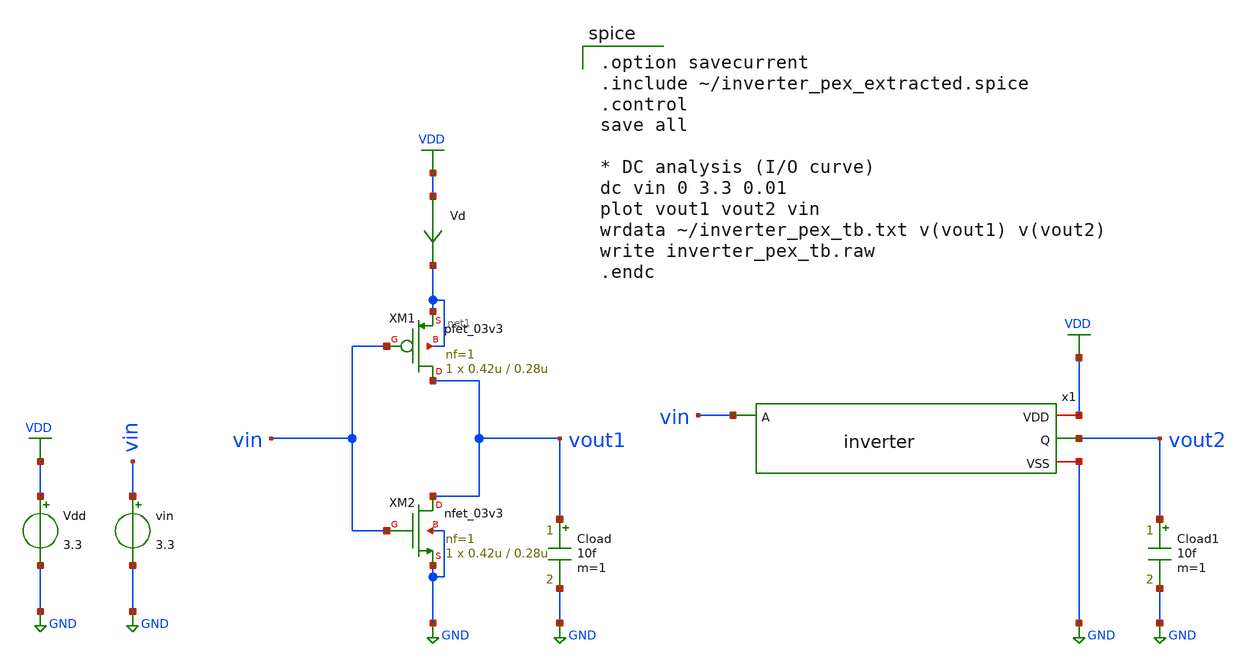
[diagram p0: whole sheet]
** sch_path: samples/inverter/GF180/inverter_pex_tb.sch
**.subckt inverter_pex_tb
Vdd VDD GND 3.3
vin vin GND 3.3
Vd VDD net1 0
.save i(vd)
Cload vout1 GND 10f m=1
x1 vin vout2 VDD GND inverter
Cload1 vout2 GND 10f m=1
XM1 vout1 vin net1 net1 pfet_03v3 L=0.28u W=0.42u nf=1 ad='int((nf+1)/2) * W/nf * 0.18u' as='int((nf+2)/2) * W/nf * 0.18u'
+ pd='2*int((nf+1)/2) * (W/nf + 0.18u)' ps='2*int((nf+2)/2) * (W/nf + 0.18u)' nrd='0.18u / W' nrs='0.18u / W'
+ sa=0 sb=0 sd=0 m=1
XM2 vout1 vin GND GND nfet_03v3 L=0.28u W=0.42u nf=1 ad='int((nf+1)/2) * W/nf * 0.18u' as='int((nf+2)/2) * W/nf * 0.18u'
+ pd='2*int((nf+1)/2) * (W/nf + 0.18u)' ps='2*int((nf+2)/2) * (W/nf + 0.18u)' nrd='0.18u / W' nrs='0.18u / W'
+ sa=0 sb=0 sd=0 m=1
**** begin user architecture code

.option savecurrent
.include ~/inverter_pex_extracted.spice
.control
save all

* DC analysis (I/O curve)
dc vin 0 3.3 0.01
plot vout1 vout2 vin
wrdata ~/inverter_pex_tb.txt v(vout1) v(vout2)
write inverter_pex_tb.raw
.endc


.include $::180MCU_MODELS/design.ngspice
.lib $::180MCU_MODELS/sm141064.ngspice typical
.lib $::180MCU_MODELS/sm141064.ngspice res_typical
.lib $::180MCU_MODELS/sm141064.ngspice moscap_typical
.lib $::180MCU_MODELS/sm141064.ngspice diode_typical
* .lib $::180MCU_MODELS/sm141064.ngspice res_statistical

**** end user architecture code
**.ends
.GLOBAL GND
.GLOBAL VDD
.end
